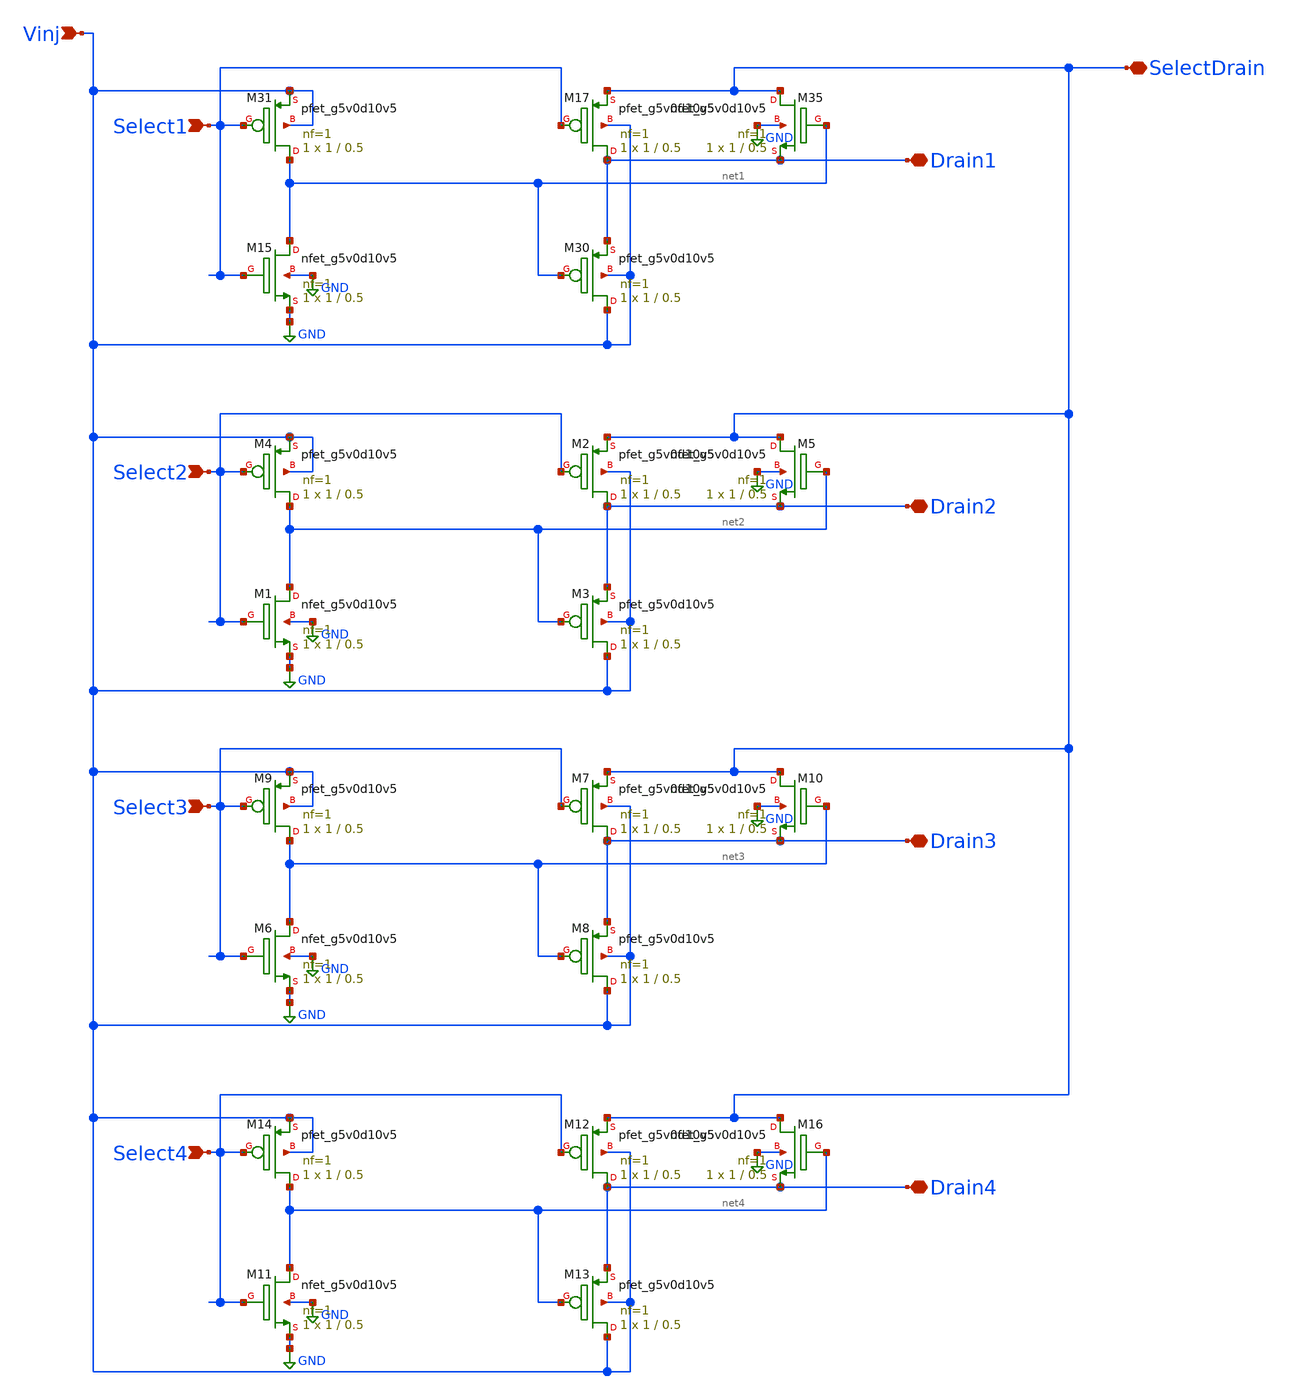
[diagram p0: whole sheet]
** sch_path: libs.ref/sky130_hilas_sc/xschem/sky130_hilas_drainSelect01.sch
**.subckt sky130_hilas_drainSelect01 Select1 SelectDrain Drain1 Vinj Select2 Drain2 Select3 Drain3
*+ Select4 Drain4
*.ipin Select1
*.iopin SelectDrain
*.iopin Drain1
*.ipin Vinj
*.ipin Select2
*.iopin Drain2
*.ipin Select3
*.iopin Drain3
*.ipin Select4
*.iopin Drain4
XM15 net1 Select1 GND GND sky130_fd_pr__nfet_g5v0d10v5 L=0.5 W=1 nf=1 ad='int((nf+1)/2) * W/nf * 0.29'
+ as='int((nf+2)/2) * W/nf * 0.29' pd='2*int((nf+1)/2) * (W/nf + 0.29)' ps='2*int((nf+2)/2) * (W/nf + 0.29)'
+ nrd='0.29 / W' nrs='0.29 / W' sa=0 sb=0 sd=0 mult=1 m=1
XM17 Drain1 Select1 SelectDrain Vinj sky130_fd_pr__pfet_g5v0d10v5 L=0.5 W=1 nf=1 ad='int((nf+1)/2) * W/nf * 0.29'
+ as='int((nf+2)/2) * W/nf * 0.29' pd='2*int((nf+1)/2) * (W/nf + 0.29)' ps='2*int((nf+2)/2) * (W/nf + 0.29)'
+ nrd='0.29 / W' nrs='0.29 / W' sa=0 sb=0 sd=0 mult=1 m=1
XM30 Vinj net1 Drain1 Vinj sky130_fd_pr__pfet_g5v0d10v5 L=0.5 W=1 nf=1 ad='int((nf+1)/2) * W/nf * 0.29'
+ as='int((nf+2)/2) * W/nf * 0.29' pd='2*int((nf+1)/2) * (W/nf + 0.29)' ps='2*int((nf+2)/2) * (W/nf + 0.29)'
+ nrd='0.29 / W' nrs='0.29 / W' sa=0 sb=0 sd=0 mult=1 m=1
XM31 net1 Select1 Vinj Vinj sky130_fd_pr__pfet_g5v0d10v5 L=0.5 W=1 nf=1 ad='int((nf+1)/2) * W/nf * 0.29'
+ as='int((nf+2)/2) * W/nf * 0.29' pd='2*int((nf+1)/2) * (W/nf + 0.29)' ps='2*int((nf+2)/2) * (W/nf + 0.29)'
+ nrd='0.29 / W' nrs='0.29 / W' sa=0 sb=0 sd=0 mult=1 m=1
XM35 SelectDrain net1 Drain1 GND sky130_fd_pr__nfet_g5v0d10v5 L=0.5 W=1 nf=1 ad='int((nf+1)/2) * W/nf * 0.29'
+ as='int((nf+2)/2) * W/nf * 0.29' pd='2*int((nf+1)/2) * (W/nf + 0.29)' ps='2*int((nf+2)/2) * (W/nf + 0.29)'
+ nrd='0.29 / W' nrs='0.29 / W' sa=0 sb=0 sd=0 mult=1 m=1
XM1 net2 Select2 GND GND sky130_fd_pr__nfet_g5v0d10v5 L=0.5 W=1 nf=1 ad='int((nf+1)/2) * W/nf * 0.29'
+ as='int((nf+2)/2) * W/nf * 0.29' pd='2*int((nf+1)/2) * (W/nf + 0.29)' ps='2*int((nf+2)/2) * (W/nf + 0.29)'
+ nrd='0.29 / W' nrs='0.29 / W' sa=0 sb=0 sd=0 mult=1 m=1
XM2 Drain2 Select2 SelectDrain Vinj sky130_fd_pr__pfet_g5v0d10v5 L=0.5 W=1 nf=1 ad='int((nf+1)/2) * W/nf * 0.29'
+ as='int((nf+2)/2) * W/nf * 0.29' pd='2*int((nf+1)/2) * (W/nf + 0.29)' ps='2*int((nf+2)/2) * (W/nf + 0.29)'
+ nrd='0.29 / W' nrs='0.29 / W' sa=0 sb=0 sd=0 mult=1 m=1
XM3 Vinj net2 Drain2 Vinj sky130_fd_pr__pfet_g5v0d10v5 L=0.5 W=1 nf=1 ad='int((nf+1)/2) * W/nf * 0.29'
+ as='int((nf+2)/2) * W/nf * 0.29' pd='2*int((nf+1)/2) * (W/nf + 0.29)' ps='2*int((nf+2)/2) * (W/nf + 0.29)'
+ nrd='0.29 / W' nrs='0.29 / W' sa=0 sb=0 sd=0 mult=1 m=1
XM4 net2 Select2 Vinj Vinj sky130_fd_pr__pfet_g5v0d10v5 L=0.5 W=1 nf=1 ad='int((nf+1)/2) * W/nf * 0.29'
+ as='int((nf+2)/2) * W/nf * 0.29' pd='2*int((nf+1)/2) * (W/nf + 0.29)' ps='2*int((nf+2)/2) * (W/nf + 0.29)'
+ nrd='0.29 / W' nrs='0.29 / W' sa=0 sb=0 sd=0 mult=1 m=1
XM5 SelectDrain net2 Drain2 GND sky130_fd_pr__nfet_g5v0d10v5 L=0.5 W=1 nf=1 ad='int((nf+1)/2) * W/nf * 0.29'
+ as='int((nf+2)/2) * W/nf * 0.29' pd='2*int((nf+1)/2) * (W/nf + 0.29)' ps='2*int((nf+2)/2) * (W/nf + 0.29)'
+ nrd='0.29 / W' nrs='0.29 / W' sa=0 sb=0 sd=0 mult=1 m=1
XM6 net3 Select3 GND GND sky130_fd_pr__nfet_g5v0d10v5 L=0.5 W=1 nf=1 ad='int((nf+1)/2) * W/nf * 0.29'
+ as='int((nf+2)/2) * W/nf * 0.29' pd='2*int((nf+1)/2) * (W/nf + 0.29)' ps='2*int((nf+2)/2) * (W/nf + 0.29)'
+ nrd='0.29 / W' nrs='0.29 / W' sa=0 sb=0 sd=0 mult=1 m=1
XM7 Drain3 Select3 SelectDrain Vinj sky130_fd_pr__pfet_g5v0d10v5 L=0.5 W=1 nf=1 ad='int((nf+1)/2) * W/nf * 0.29'
+ as='int((nf+2)/2) * W/nf * 0.29' pd='2*int((nf+1)/2) * (W/nf + 0.29)' ps='2*int((nf+2)/2) * (W/nf + 0.29)'
+ nrd='0.29 / W' nrs='0.29 / W' sa=0 sb=0 sd=0 mult=1 m=1
XM8 Vinj net3 Drain3 Vinj sky130_fd_pr__pfet_g5v0d10v5 L=0.5 W=1 nf=1 ad='int((nf+1)/2) * W/nf * 0.29'
+ as='int((nf+2)/2) * W/nf * 0.29' pd='2*int((nf+1)/2) * (W/nf + 0.29)' ps='2*int((nf+2)/2) * (W/nf + 0.29)'
+ nrd='0.29 / W' nrs='0.29 / W' sa=0 sb=0 sd=0 mult=1 m=1
XM9 net3 Select3 Vinj Vinj sky130_fd_pr__pfet_g5v0d10v5 L=0.5 W=1 nf=1 ad='int((nf+1)/2) * W/nf * 0.29'
+ as='int((nf+2)/2) * W/nf * 0.29' pd='2*int((nf+1)/2) * (W/nf + 0.29)' ps='2*int((nf+2)/2) * (W/nf + 0.29)'
+ nrd='0.29 / W' nrs='0.29 / W' sa=0 sb=0 sd=0 mult=1 m=1
XM10 SelectDrain net3 Drain3 GND sky130_fd_pr__nfet_g5v0d10v5 L=0.5 W=1 nf=1 ad='int((nf+1)/2) * W/nf * 0.29'
+ as='int((nf+2)/2) * W/nf * 0.29' pd='2*int((nf+1)/2) * (W/nf + 0.29)' ps='2*int((nf+2)/2) * (W/nf + 0.29)'
+ nrd='0.29 / W' nrs='0.29 / W' sa=0 sb=0 sd=0 mult=1 m=1
XM11 net4 Select4 GND GND sky130_fd_pr__nfet_g5v0d10v5 L=0.5 W=1 nf=1 ad='int((nf+1)/2) * W/nf * 0.29'
+ as='int((nf+2)/2) * W/nf * 0.29' pd='2*int((nf+1)/2) * (W/nf + 0.29)' ps='2*int((nf+2)/2) * (W/nf + 0.29)'
+ nrd='0.29 / W' nrs='0.29 / W' sa=0 sb=0 sd=0 mult=1 m=1
XM12 Drain4 Select4 SelectDrain Vinj sky130_fd_pr__pfet_g5v0d10v5 L=0.5 W=1 nf=1 ad='int((nf+1)/2) * W/nf * 0.29'
+ as='int((nf+2)/2) * W/nf * 0.29' pd='2*int((nf+1)/2) * (W/nf + 0.29)' ps='2*int((nf+2)/2) * (W/nf + 0.29)'
+ nrd='0.29 / W' nrs='0.29 / W' sa=0 sb=0 sd=0 mult=1 m=1
XM13 Vinj net4 Drain4 Vinj sky130_fd_pr__pfet_g5v0d10v5 L=0.5 W=1 nf=1 ad='int((nf+1)/2) * W/nf * 0.29'
+ as='int((nf+2)/2) * W/nf * 0.29' pd='2*int((nf+1)/2) * (W/nf + 0.29)' ps='2*int((nf+2)/2) * (W/nf + 0.29)'
+ nrd='0.29 / W' nrs='0.29 / W' sa=0 sb=0 sd=0 mult=1 m=1
XM14 net4 Select4 Vinj Vinj sky130_fd_pr__pfet_g5v0d10v5 L=0.5 W=1 nf=1 ad='int((nf+1)/2) * W/nf * 0.29'
+ as='int((nf+2)/2) * W/nf * 0.29' pd='2*int((nf+1)/2) * (W/nf + 0.29)' ps='2*int((nf+2)/2) * (W/nf + 0.29)'
+ nrd='0.29 / W' nrs='0.29 / W' sa=0 sb=0 sd=0 mult=1 m=1
XM16 SelectDrain net4 Drain4 GND sky130_fd_pr__nfet_g5v0d10v5 L=0.5 W=1 nf=1 ad='int((nf+1)/2) * W/nf * 0.29'
+ as='int((nf+2)/2) * W/nf * 0.29' pd='2*int((nf+1)/2) * (W/nf + 0.29)' ps='2*int((nf+2)/2) * (W/nf + 0.29)'
+ nrd='0.29 / W' nrs='0.29 / W' sa=0 sb=0 sd=0 mult=1 m=1
**.ends
.GLOBAL GND
.end
